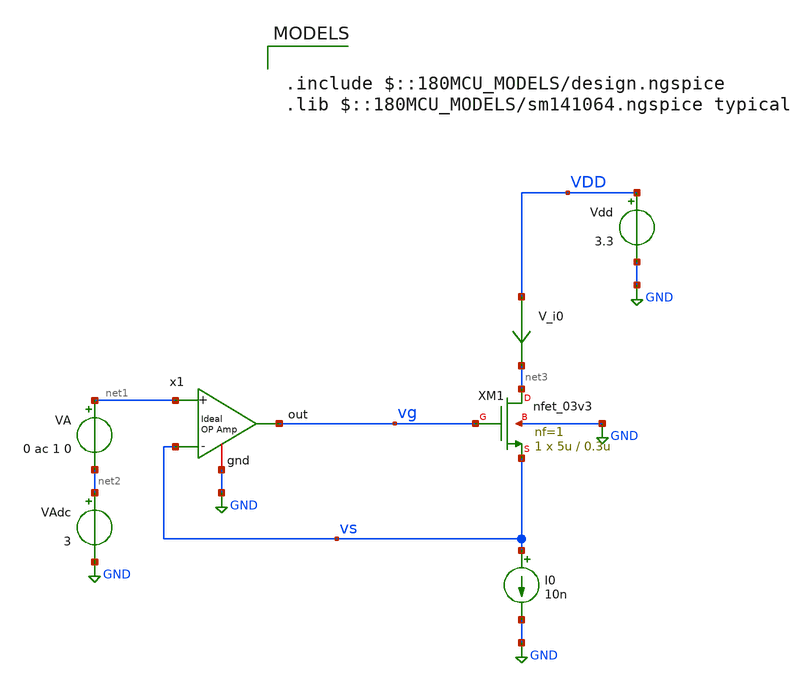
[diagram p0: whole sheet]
** sch_path: New_Extraction/nmos_n_ext.sch
**.subckt nmos_n_ext
x1 vg net1 vs GND ampOp_ideal
XM1 net3 vg vs GND nfet_03v3 L=0.3u W=5u nf=1 ad='int((nf+1)/2) * W/nf * 0.18u' as='int((nf+2)/2) * W/nf * 0.18u'
+ pd='2*int((nf+1)/2) * (W/nf + 0.18u)' ps='2*int((nf+2)/2) * (W/nf + 0.18u)' nrd='0.18u / W' nrs='0.18u / W'
+ sa=0 sb=0 sd=0 m=1
I0 vs GND 10n
V_i0 VDD net3 0
.save i(v_i0)
VA net1 net2 0 ac 1 0
VAdc net2 GND 3
Vdd VDD GND 3.3
**** begin user architecture code

.include $::180MCU_MODELS/design.ngspice
.lib $::180MCU_MODELS/sm141064.ngspice typical



.option savecurrents

.control
  save all
  op
  remzerovec
  write nmos_n_ext.raw
  set appendwrite

  ac dec 100 1 1e10
  let n_vec= vg/vs

  meas ac n FIND n_vec AT=10

  echo
  echo
  echo
  echo Extracted n:
  print n
  echo
  echo
  echo

  remzerovec
  write nmos_n_ext.raw


.endc
.save all


**** end user architecture code
**.ends

* expanding   symbol:  /home/gmaranhao/Desktop/gf180_work/auxLib/ampOp_ideal.sym # of pins=4
** sym_path: gf_tutorials/auxLib/ampOp_ideal.sym
** sch_path: gf_tutorials/auxLib/ampOp_ideal.sch
.subckt ampOp_ideal out + - gnd
*.ipin +
*.ipin -
*.opin out
*.iopin gnd
E1 out gnd + - 10000000
.ends

.GLOBAL GND
.end
